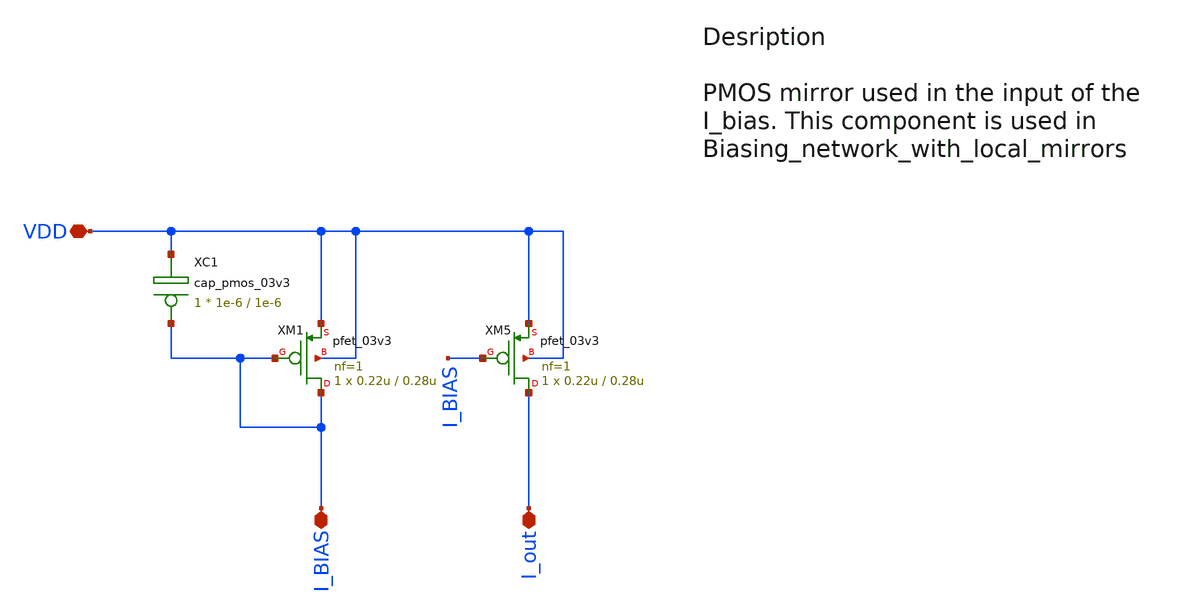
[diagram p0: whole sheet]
** sch_path: src/design_xsch/Local_mirror_pmos.sch
**.subckt Local_mirror_pmos I_BIAS VDD I_out
*.iopin I_BIAS
*.iopin VDD
*.iopin I_out
XM1 I_BIAS I_BIAS VDD VDD pfet_03v3 L=0.28u W=0.22u nf=1 ad='int((nf+1)/2) * W/nf * 0.18u' as='int((nf+2)/2) * W/nf * 0.18u'
+ pd='2*int((nf+1)/2) * (W/nf + 0.18u)' ps='2*int((nf+2)/2) * (W/nf + 0.18u)' nrd='0.18u / W' nrs='0.18u / W'
+ sa=0 sb=0 sd=0 m=1
XM5 I_out I_BIAS VDD VDD pfet_03v3 L=0.28u W=0.22u nf=1 ad='int((nf+1)/2) * W/nf * 0.18u' as='int((nf+2)/2) * W/nf * 0.18u'
+ pd='2*int((nf+1)/2) * (W/nf + 0.18u)' ps='2*int((nf+2)/2) * (W/nf + 0.18u)' nrd='0.18u / W' nrs='0.18u / W'
+ sa=0 sb=0 sd=0 m=1
XC1 I_BIAS VDD cap_pmos_03v3 c_width=1e-6 c_length=1e-6 m=1
**** begin user architecture code

.include $::180MCU_MODELS/design.ngspice
.lib $::180MCU_MODELS/sm141064.ngspice typical
.lib $::180MCU_MODELS/sm141064.ngspice mimcap_typical
.lib $::180MCU_MODELS/sm141064.ngspice cap_mim
.lib $::180MCU_MODELS/sm141064.ngspice res_typical




* let sets vectors to a plot, while set sets a variable, globally accessible in .control
.control

    * Set frequency and amplitude variables to proper values from within the control sequence
    save all

    op
    show

    write Biasing_network_sim.raw

    set appendwrite

    * Transient analysis to observe mixing operation
    tran 1p 10n


    write Biasing_network_sim.raw

.endc


**** end user architecture code
**.ends
.end
